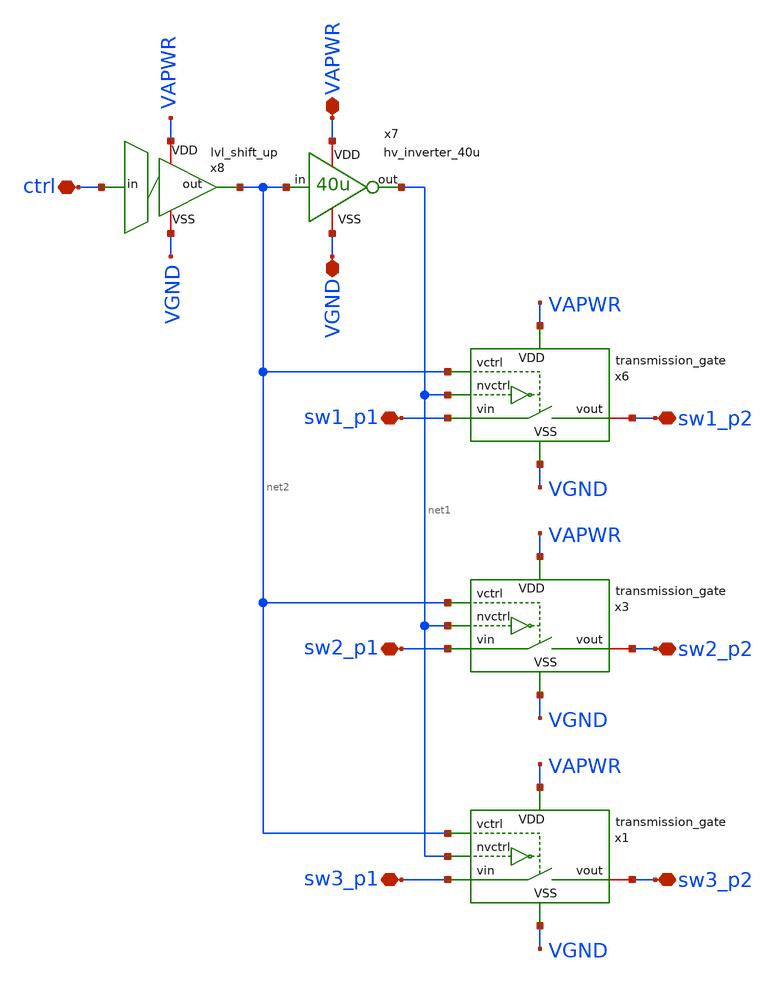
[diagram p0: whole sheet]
** sch_path: macros/heichips26_vcr/schematic/xschem/analog_switch_3pst.sch
**.subckt analog_switch_3pst sw1_p1 ctrl VAPWR VGND sw2_p1 sw1_p2 sw2_p2 sw3_p1 sw3_p2
*.iopin sw1_p1
*.iopin ctrl
*.iopin VAPWR
*.iopin VGND
*.iopin sw2_p1
*.iopin sw1_p2
*.iopin sw2_p2
*.iopin sw3_p1
*.iopin sw3_p2
x6 net2 sw1_p1 sw1_p2 net1 VAPWR VGND transmission_gate
x7 VAPWR net2 net1 VGND hv_inverter_40u
x3 net2 sw2_p1 sw2_p2 net1 VAPWR VGND transmission_gate
x8 VAPWR ctrl net2 VGND lvl_shift_up
x1 net2 sw3_p1 sw3_p2 net1 VAPWR VGND transmission_gate
**.ends

* expanding   symbol:
*+  /home/noah/Documents/freizeit/heichips/heichips26-voltage-controlled-resistor/macros/heichips26_vcr/macros/switched_capacitor/schematic/xschem/transmission_gate.sym # of pins=6
** sym_path: macros/heichips26_vcr/macros/switched_capacitor/schematic/xschem/transmission_gate.sym
** sch_path: macros/heichips26_vcr/macros/switched_capacitor/schematic/xschem/transmission_gate.sch
.subckt transmission_gate vctrl vin vout nvctrl VDD VSS
*.iopin vin
*.iopin vout
*.ipin vctrl
*.ipin nvctrl
*.iopin VDD
*.iopin VSS
XM3 vout vctrl vin VSS sg13_hv_nmos w={tg_ngate_w*tg_ng} l={tg_ch_len} ng={tg_ng} m=1 mm_ok=1
XM4 vout nvctrl vin VDD sg13_hv_pmos w={tg_pgate_w*tg_ng} l={tg_ch_len} ng={tg_ng} m=1 mm_ok=1
**** begin user architecture code


.param tg_ch_len=1u
.param tg_ngate_w=2u
.param tg_pgate_w=10u
.param tg_ng=20


**** end user architecture code
.ends


* expanding   symbol:
*+  /home/noah/Documents/freizeit/heichips/heichips26-voltage-controlled-resistor/macros/heichips26_vcr/macros/switched_capacitor/schematic/xschem/hv_inverter_40u.sym # of pins=4
** sym_path: macros/heichips26_vcr/macros/switched_capacitor/schematic/xschem/hv_inverter_40u.sym
** sch_path: macros/heichips26_vcr/macros/switched_capacitor/schematic/xschem/hv_inverter_40u.sch
.subckt hv_inverter_40u VDD in out VSS
*.ipin in
*.iopin VDD
*.iopin VSS
*.opin out
XM2 out in VSS VSS sg13_hv_nmos w={n_w} l={n_l} ng={ng} m=1 mm_ok=1
XM3 out in VDD VDD sg13_hv_pmos w={p_w} l={p_l} ng={ng} m=1 mm_ok=1
**** begin user architecture code


.param w   = 10u
.param ng  = 4
.param n_ng = ng
.param n_w = {3u*n_ng}
.param n_l = 0.45u
.param p_ng = ng
.param p_w = {10u*p_ng}
.param p_l = 0.4u


**** end user architecture code
.ends


* expanding   symbol:
*+  /home/noah/Documents/freizeit/heichips/heichips26-voltage-controlled-resistor/macros/heichips26_vcr/macros/switched_capacitor/schematic/xschem/lvl_shift_up.sym # of pins=4
** sym_path: macros/heichips26_vcr/macros/switched_capacitor/schematic/xschem/lvl_shift_up.sym
** sch_path: macros/heichips26_vcr/macros/switched_capacitor/schematic/xschem/lvl_shift_up.sch
.subckt lvl_shift_up VDD in out VSS
*.ipin in
*.iopin VDD
*.iopin VSS
*.opin out
XM1 net1 in VSS VSS sg13_hv_nmos w={n_ng*n_w} l={n_l} ng={n_ng} m=1 mm_ok=1
XM2 net1 in VDD VDD sg13_hv_pmos w={p_ng*p_w} l={p_l} ng={n_ng} m=1 mm_ok=1
**** begin user architecture code


.param n_ng = 2
.param n_w = 10u
.param n_l = 0.45u
.param p_ng = 2
.param p_w = 1u
.param p_l = 0.45u


**** end user architecture code
x4 VDD net1 out VSS hv_inverter_6u5
.ends


* expanding   symbol:  hv_inverter_6u5.sym # of pins=4
** sym_path: macros/heichips26_vcr/macros/switched_capacitor/schematic/xschem/hv_inverter_6u5.sym
** sch_path: macros/heichips26_vcr/macros/switched_capacitor/schematic/xschem/hv_inverter_6u5.sch
.subckt hv_inverter_6u5 VDD in out VSS
*.ipin in
*.iopin VDD
*.iopin VSS
*.opin out
XM2 out in VSS VSS sg13_hv_nmos w={n_w} l={n_l} ng={ng} m=1 mm_ok=1
XM3 out in VDD VDD sg13_hv_pmos w={p_w} l={p_l} ng={ng} m=1 mm_ok=1
**** begin user architecture code


.param ng  = 1
.param n_ng = ng
.param n_w = {2u*n_ng}
.param n_l = 0.45u
.param p_ng = ng
.param p_w = {6.5u*p_ng}
.param p_l = 0.4u


**** end user architecture code
.ends

.end
